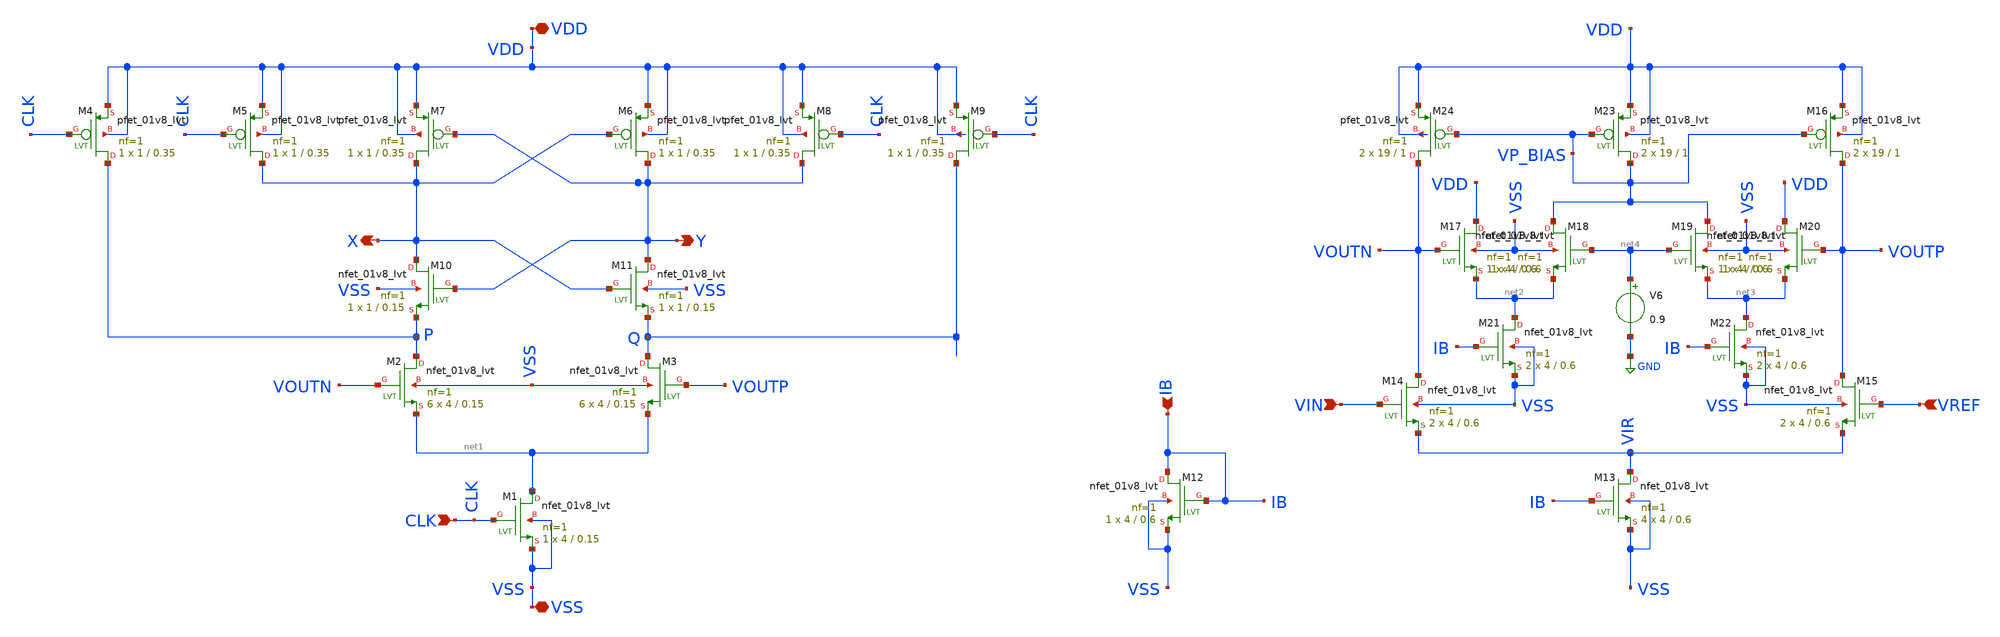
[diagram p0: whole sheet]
** sch_path: strongARM/strongARM_v3_sym.sch
**.subckt strongARM_v3_sym IB CLK VSS VDD Y X VIN VREF
*.ipin IB
*.ipin CLK
*.iopin VSS
*.iopin VDD
*.opin Y
*.opin X
*.ipin VIN
*.ipin VREF
XM2 P VOUTN net1 VSS sky130_fd_pr__nfet_01v8_lvt L=0.15 W=4 nf=1 ad='int((nf+1)/2) * W/nf * 0.29' as='int((nf+2)/2) * W/nf * 0.29'
+ pd='2*int((nf+1)/2) * (W/nf + 0.29)' ps='2*int((nf+2)/2) * (W/nf + 0.29)' nrd='0.29 / W' nrs='0.29 / W'
+ sa=0 sb=0 sd=0 mult=6 m=6
XM3 Q VOUTP net1 VSS sky130_fd_pr__nfet_01v8_lvt L=0.15 W=4 nf=1 ad='int((nf+1)/2) * W/nf * 0.29' as='int((nf+2)/2) * W/nf * 0.29'
+ pd='2*int((nf+1)/2) * (W/nf + 0.29)' ps='2*int((nf+2)/2) * (W/nf + 0.29)' nrd='0.29 / W' nrs='0.29 / W'
+ sa=0 sb=0 sd=0 mult=6 m=6
XM4 P CLK VDD VDD sky130_fd_pr__pfet_01v8_lvt L=0.35 W=1 nf=1 ad='int((nf+1)/2) * W/nf * 0.29' as='int((nf+2)/2) * W/nf * 0.29'
+ pd='2*int((nf+1)/2) * (W/nf + 0.29)' ps='2*int((nf+2)/2) * (W/nf + 0.29)' nrd='0.29 / W' nrs='0.29 / W'
+ sa=0 sb=0 sd=0 mult=1 m=1
XM5 X CLK VDD VDD sky130_fd_pr__pfet_01v8_lvt L=0.35 W=1 nf=1 ad='int((nf+1)/2) * W/nf * 0.29' as='int((nf+2)/2) * W/nf * 0.29'
+ pd='2*int((nf+1)/2) * (W/nf + 0.29)' ps='2*int((nf+2)/2) * (W/nf + 0.29)' nrd='0.29 / W' nrs='0.29 / W'
+ sa=0 sb=0 sd=0 mult=1 m=1
XM6 Y X VDD VDD sky130_fd_pr__pfet_01v8_lvt L=0.35 W=1 nf=1 ad='int((nf+1)/2) * W/nf * 0.29' as='int((nf+2)/2) * W/nf * 0.29'
+ pd='2*int((nf+1)/2) * (W/nf + 0.29)' ps='2*int((nf+2)/2) * (W/nf + 0.29)' nrd='0.29 / W' nrs='0.29 / W'
+ sa=0 sb=0 sd=0 mult=1 m=1
XM7 X Y VDD VDD sky130_fd_pr__pfet_01v8_lvt L=0.35 W=1 nf=1 ad='int((nf+1)/2) * W/nf * 0.29' as='int((nf+2)/2) * W/nf * 0.29'
+ pd='2*int((nf+1)/2) * (W/nf + 0.29)' ps='2*int((nf+2)/2) * (W/nf + 0.29)' nrd='0.29 / W' nrs='0.29 / W'
+ sa=0 sb=0 sd=0 mult=1 m=1
XM8 Y CLK VDD VDD sky130_fd_pr__pfet_01v8_lvt L=0.35 W=1 nf=1 ad='int((nf+1)/2) * W/nf * 0.29' as='int((nf+2)/2) * W/nf * 0.29'
+ pd='2*int((nf+1)/2) * (W/nf + 0.29)' ps='2*int((nf+2)/2) * (W/nf + 0.29)' nrd='0.29 / W' nrs='0.29 / W'
+ sa=0 sb=0 sd=0 mult=1 m=1
XM9 Q CLK VDD VDD sky130_fd_pr__pfet_01v8_lvt L=0.35 W=1 nf=1 ad='int((nf+1)/2) * W/nf * 0.29' as='int((nf+2)/2) * W/nf * 0.29'
+ pd='2*int((nf+1)/2) * (W/nf + 0.29)' ps='2*int((nf+2)/2) * (W/nf + 0.29)' nrd='0.29 / W' nrs='0.29 / W'
+ sa=0 sb=0 sd=0 mult=1 m=1
XM10 X Y P VSS sky130_fd_pr__nfet_01v8_lvt L=0.15 W=1 nf=1 ad='int((nf+1)/2) * W/nf * 0.29' as='int((nf+2)/2) * W/nf * 0.29'
+ pd='2*int((nf+1)/2) * (W/nf + 0.29)' ps='2*int((nf+2)/2) * (W/nf + 0.29)' nrd='0.29 / W' nrs='0.29 / W'
+ sa=0 sb=0 sd=0 mult=1 m=1
XM11 Y X Q VSS sky130_fd_pr__nfet_01v8_lvt L=0.15 W=1 nf=1 ad='int((nf+1)/2) * W/nf * 0.29' as='int((nf+2)/2) * W/nf * 0.29'
+ pd='2*int((nf+1)/2) * (W/nf + 0.29)' ps='2*int((nf+2)/2) * (W/nf + 0.29)' nrd='0.29 / W' nrs='0.29 / W'
+ sa=0 sb=0 sd=0 mult=1 m=1
XM1 net1 CLK VSS VSS sky130_fd_pr__nfet_01v8_lvt L=0.15 W=4 nf=1 ad='int((nf+1)/2) * W/nf * 0.29' as='int((nf+2)/2) * W/nf * 0.29'
+ pd='2*int((nf+1)/2) * (W/nf + 0.29)' ps='2*int((nf+2)/2) * (W/nf + 0.29)' nrd='0.29 / W' nrs='0.29 / W'
+ sa=0 sb=0 sd=0 mult=1 m=1
XM12 IB IB VSS VSS sky130_fd_pr__nfet_01v8_lvt L=0.6 W=4 nf=1 ad='int((nf+1)/2) * W/nf * 0.29' as='int((nf+2)/2) * W/nf * 0.29'
+ pd='2*int((nf+1)/2) * (W/nf + 0.29)' ps='2*int((nf+2)/2) * (W/nf + 0.29)' nrd='0.29 / W' nrs='0.29 / W'
+ sa=0 sb=0 sd=0 mult=1 m=1
XM13 VIR IB VSS VSS sky130_fd_pr__nfet_01v8_lvt L=0.6 W=4 nf=1 ad='int((nf+1)/2) * W/nf * 0.29' as='int((nf+2)/2) * W/nf * 0.29'
+ pd='2*int((nf+1)/2) * (W/nf + 0.29)' ps='2*int((nf+2)/2) * (W/nf + 0.29)' nrd='0.29 / W' nrs='0.29 / W'
+ sa=0 sb=0 sd=0 mult=4 m=4
XM14 VOUTN VIN VIR VSS sky130_fd_pr__nfet_01v8_lvt L=0.6 W=4 nf=1 ad='int((nf+1)/2) * W/nf * 0.29' as='int((nf+2)/2) * W/nf * 0.29'
+ pd='2*int((nf+1)/2) * (W/nf + 0.29)' ps='2*int((nf+2)/2) * (W/nf + 0.29)' nrd='0.29 / W' nrs='0.29 / W'
+ sa=0 sb=0 sd=0 mult=2 m=2
XM15 VOUTP VREF VIR VSS sky130_fd_pr__nfet_01v8_lvt L=0.6 W=4 nf=1 ad='int((nf+1)/2) * W/nf * 0.29' as='int((nf+2)/2) * W/nf * 0.29'
+ pd='2*int((nf+1)/2) * (W/nf + 0.29)' ps='2*int((nf+2)/2) * (W/nf + 0.29)' nrd='0.29 / W' nrs='0.29 / W'
+ sa=0 sb=0 sd=0 mult=2 m=2
XM16 VOUTP VP_BIAS VDD VDD sky130_fd_pr__pfet_01v8_lvt L=1 W=19 nf=1 ad='int((nf+1)/2) * W/nf * 0.29'
+ as='int((nf+2)/2) * W/nf * 0.29' pd='2*int((nf+1)/2) * (W/nf + 0.29)' ps='2*int((nf+2)/2) * (W/nf + 0.29)'
+ nrd='0.29 / W' nrs='0.29 / W' sa=0 sb=0 sd=0 mult=2 m=2
XM17 VDD VOUTN net2 VSS sky130_fd_pr__nfet_01v8_lvt L=0.6 W=4 nf=1 ad='int((nf+1)/2) * W/nf * 0.29' as='int((nf+2)/2) * W/nf * 0.29'
+ pd='2*int((nf+1)/2) * (W/nf + 0.29)' ps='2*int((nf+2)/2) * (W/nf + 0.29)' nrd='0.29 / W' nrs='0.29 / W'
+ sa=0 sb=0 sd=0 mult=1 m=1
XM18 VP_BIAS net4 net2 VSS sky130_fd_pr__nfet_01v8_lvt L=0.6 W=4 nf=1 ad='int((nf+1)/2) * W/nf * 0.29'
+ as='int((nf+2)/2) * W/nf * 0.29' pd='2*int((nf+1)/2) * (W/nf + 0.29)' ps='2*int((nf+2)/2) * (W/nf + 0.29)'
+ nrd='0.29 / W' nrs='0.29 / W' sa=0 sb=0 sd=0 mult=1 m=1
XM19 VP_BIAS net4 net3 VSS sky130_fd_pr__nfet_01v8_lvt L=0.6 W=4 nf=1 ad='int((nf+1)/2) * W/nf * 0.29'
+ as='int((nf+2)/2) * W/nf * 0.29' pd='2*int((nf+1)/2) * (W/nf + 0.29)' ps='2*int((nf+2)/2) * (W/nf + 0.29)'
+ nrd='0.29 / W' nrs='0.29 / W' sa=0 sb=0 sd=0 mult=1 m=1
XM20 VDD VOUTP net3 VSS sky130_fd_pr__nfet_01v8_lvt L=0.6 W=4 nf=1 ad='int((nf+1)/2) * W/nf * 0.29' as='int((nf+2)/2) * W/nf * 0.29'
+ pd='2*int((nf+1)/2) * (W/nf + 0.29)' ps='2*int((nf+2)/2) * (W/nf + 0.29)' nrd='0.29 / W' nrs='0.29 / W'
+ sa=0 sb=0 sd=0 mult=1 m=1
XM21 net2 IB VSS VSS sky130_fd_pr__nfet_01v8_lvt L=0.6 W=4 nf=1 ad='int((nf+1)/2) * W/nf * 0.29' as='int((nf+2)/2) * W/nf * 0.29'
+ pd='2*int((nf+1)/2) * (W/nf + 0.29)' ps='2*int((nf+2)/2) * (W/nf + 0.29)' nrd='0.29 / W' nrs='0.29 / W'
+ sa=0 sb=0 sd=0 mult=2 m=2
XM22 net3 IB VSS VSS sky130_fd_pr__nfet_01v8_lvt L=0.6 W=4 nf=1 ad='int((nf+1)/2) * W/nf * 0.29' as='int((nf+2)/2) * W/nf * 0.29'
+ pd='2*int((nf+1)/2) * (W/nf + 0.29)' ps='2*int((nf+2)/2) * (W/nf + 0.29)' nrd='0.29 / W' nrs='0.29 / W'
+ sa=0 sb=0 sd=0 mult=2 m=2
XM23 VP_BIAS VP_BIAS VDD VDD sky130_fd_pr__pfet_01v8_lvt L=1 W=19 nf=1 ad='int((nf+1)/2) * W/nf * 0.29'
+ as='int((nf+2)/2) * W/nf * 0.29' pd='2*int((nf+1)/2) * (W/nf + 0.29)' ps='2*int((nf+2)/2) * (W/nf + 0.29)'
+ nrd='0.29 / W' nrs='0.29 / W' sa=0 sb=0 sd=0 mult=2 m=2
V6 net4 GND 0.9
XM24 VOUTN VP_BIAS VDD VDD sky130_fd_pr__pfet_01v8_lvt L=1 W=19 nf=1 ad='int((nf+1)/2) * W/nf * 0.29'
+ as='int((nf+2)/2) * W/nf * 0.29' pd='2*int((nf+1)/2) * (W/nf + 0.29)' ps='2*int((nf+2)/2) * (W/nf + 0.29)'
+ nrd='0.29 / W' nrs='0.29 / W' sa=0 sb=0 sd=0 mult=2 m=2
**.ends
.GLOBAL GND
.end
